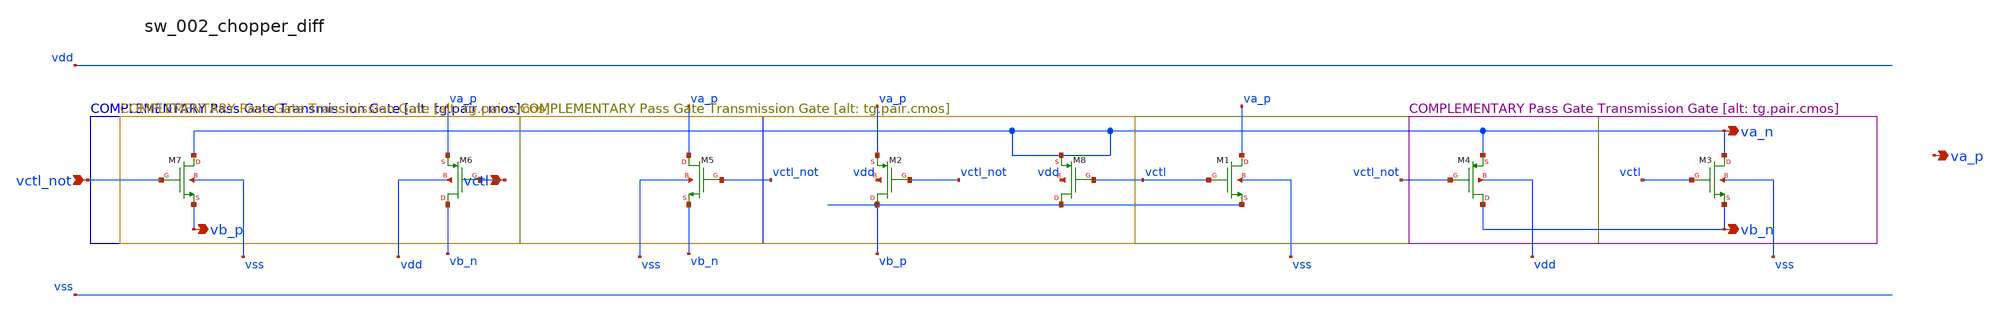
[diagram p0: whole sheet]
** sch_path: analog-db/raw/sw_002_chopper_diff/sw_002_chopper_diff_annotated.sch
**.subckt sw_002_chopper_diff_annotated vctl_not vctl va_n vb_p vb_n va_p
*.ipin vctl_not
*.ipin vctl
*.opin va_n
*.opin vb_p
*.opin vb_n
*.opin va_p
XM1 va_p vctl vb_p vss sg13_lv_nmos w=x_dut_xm1_w l=x_dut_xm1_l ng=1 m=x_dut_xm1_m
XM2 vb_p vctl_not va_p vdd sg13_lv_pmos w=x_dut_xm2_w l=x_dut_xm2_l ng=1 m=x_dut_xm2_m
XM3 va_n vctl vb_n vss sg13_lv_nmos w=x_dut_xm3_w l=x_dut_xm3_l ng=1 m=x_dut_xm3_m
XM4 vb_n vctl_not va_n vdd sg13_lv_pmos w=x_dut_xm4_w l=x_dut_xm4_l ng=1 m=x_dut_xm4_m
XM5 va_p vctl_not vb_n vss sg13_lv_nmos w=x_dut_xm5_w l=x_dut_xm5_l ng=1 m=x_dut_xm5_m
XM6 vb_n vctl va_p vdd sg13_lv_pmos w=x_dut_xm6_w l=x_dut_xm6_l ng=1 m=x_dut_xm6_m
XM7 va_n vctl_not vb_p vss sg13_lv_nmos w=x_dut_xm7_w l=x_dut_xm7_l ng=1 m=x_dut_xm7_m
XM8 vb_p vctl va_n vdd sg13_lv_pmos w=x_dut_xm8_w l=x_dut_xm8_l ng=1 m=x_dut_xm8_m
**.ends
.end
